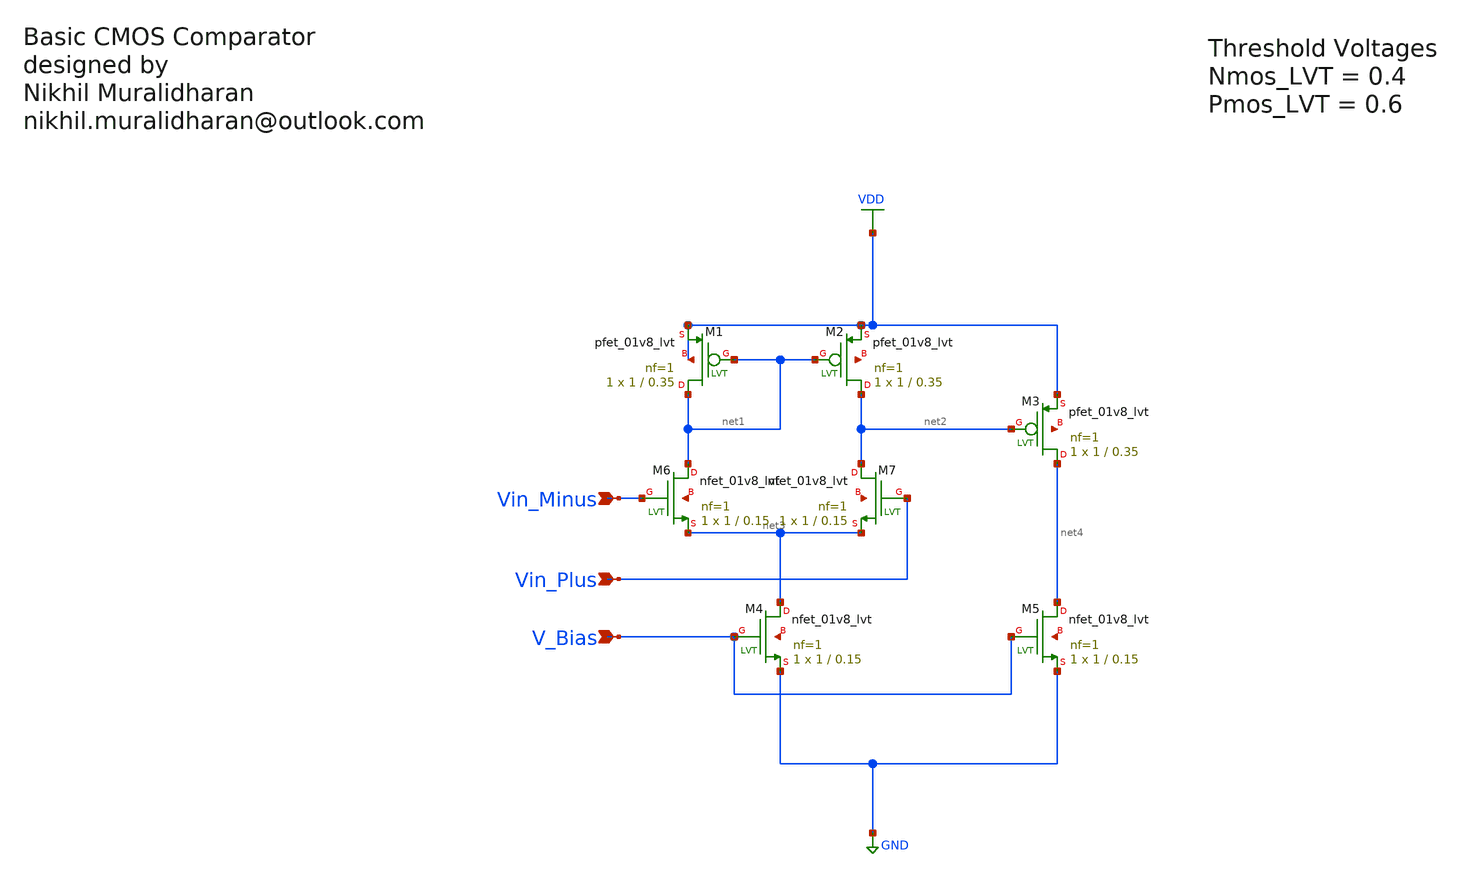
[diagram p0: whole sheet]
** sch_path: Current Sensor/Comparator.sch
**.subckt Comparator V_Bias Vin_Plus Vin_Minus
*.ipin V_Bias
*.ipin Vin_Plus
*.ipin Vin_Minus
XM1 net1 net1 VDD VDD sky130_fd_pr__pfet_01v8_lvt L=0.35 W=1 nf=1 ad='int((nf+1)/2) * W/nf * 0.29' as='int((nf+2)/2) * W/nf * 0.29'
+ pd='2*int((nf+1)/2) * (W/nf + 0.29)' ps='2*int((nf+2)/2) * (W/nf + 0.29)' nrd='0.29 / W' nrs='0.29 / W'
+ sa=0 sb=0 sd=0 mult=1 m=1
XM2 net2 net1 VDD net5 sky130_fd_pr__pfet_01v8_lvt L=0.35 W=1 nf=1 ad='int((nf+1)/2) * W/nf * 0.29' as='int((nf+2)/2) * W/nf * 0.29'
+ pd='2*int((nf+1)/2) * (W/nf + 0.29)' ps='2*int((nf+2)/2) * (W/nf + 0.29)' nrd='0.29 / W' nrs='0.29 / W'
+ sa=0 sb=0 sd=0 mult=1 m=1
XM3 net4 net2 VDD net6 sky130_fd_pr__pfet_01v8_lvt L=0.35 W=1 nf=1 ad='int((nf+1)/2) * W/nf * 0.29' as='int((nf+2)/2) * W/nf * 0.29'
+ pd='2*int((nf+1)/2) * (W/nf + 0.29)' ps='2*int((nf+2)/2) * (W/nf + 0.29)' nrd='0.29 / W' nrs='0.29 / W'
+ sa=0 sb=0 sd=0 mult=1 m=1
XM4 net3 V_Bias GND net7 sky130_fd_pr__nfet_01v8_lvt L=0.15 W=1 nf=1 ad='int((nf+1)/2) * W/nf * 0.29'
+ as='int((nf+2)/2) * W/nf * 0.29' pd='2*int((nf+1)/2) * (W/nf + 0.29)' ps='2*int((nf+2)/2) * (W/nf + 0.29)'
+ nrd='0.29 / W' nrs='0.29 / W' sa=0 sb=0 sd=0 mult=1 m=1
XM5 net4 V_Bias GND net8 sky130_fd_pr__nfet_01v8_lvt L=0.15 W=1 nf=1 ad='int((nf+1)/2) * W/nf * 0.29'
+ as='int((nf+2)/2) * W/nf * 0.29' pd='2*int((nf+1)/2) * (W/nf + 0.29)' ps='2*int((nf+2)/2) * (W/nf + 0.29)'
+ nrd='0.29 / W' nrs='0.29 / W' sa=0 sb=0 sd=0 mult=1 m=1
XM6 net1 Vin_Minus net3 net9 sky130_fd_pr__nfet_01v8_lvt L=0.15 W=1 nf=1 ad='int((nf+1)/2) * W/nf * 0.29'
+ as='int((nf+2)/2) * W/nf * 0.29' pd='2*int((nf+1)/2) * (W/nf + 0.29)' ps='2*int((nf+2)/2) * (W/nf + 0.29)'
+ nrd='0.29 / W' nrs='0.29 / W' sa=0 sb=0 sd=0 mult=1 m=1
XM7 net2 Vin_Plus net3 net10 sky130_fd_pr__nfet_01v8_lvt L=0.15 W=1 nf=1 ad='int((nf+1)/2) * W/nf * 0.29'
+ as='int((nf+2)/2) * W/nf * 0.29' pd='2*int((nf+1)/2) * (W/nf + 0.29)' ps='2*int((nf+2)/2) * (W/nf + 0.29)'
+ nrd='0.29 / W' nrs='0.29 / W' sa=0 sb=0 sd=0 mult=1 m=1
**.ends
.GLOBAL VDD
.GLOBAL GND
.end
